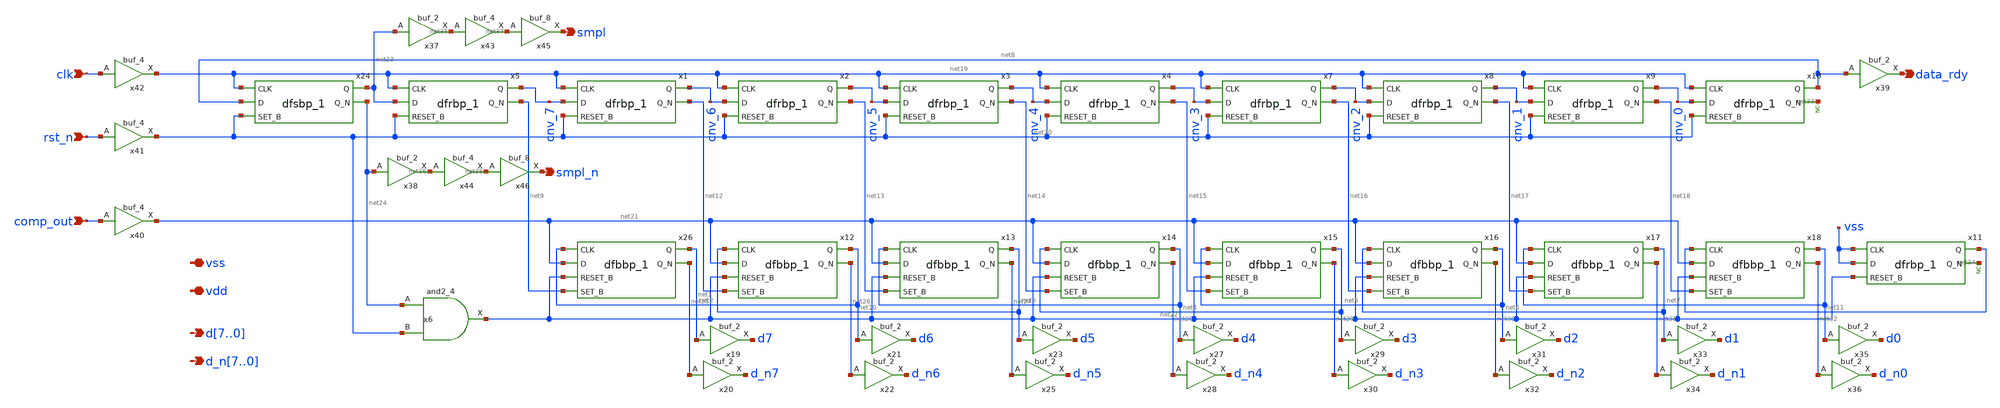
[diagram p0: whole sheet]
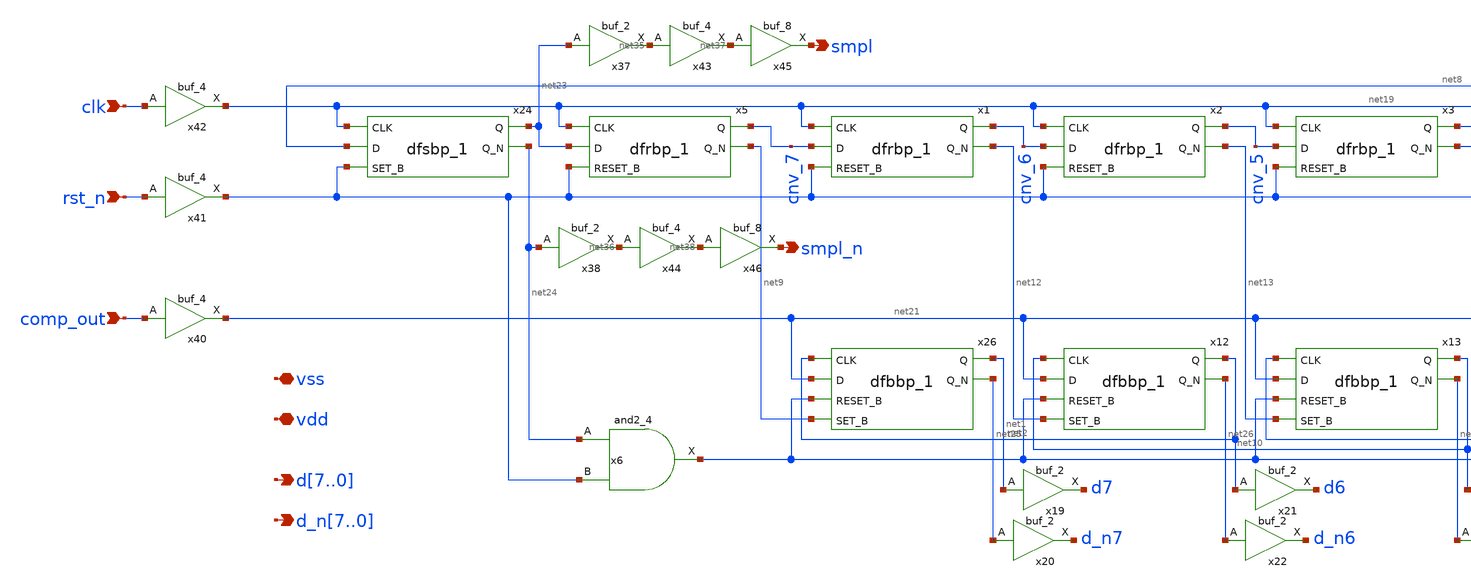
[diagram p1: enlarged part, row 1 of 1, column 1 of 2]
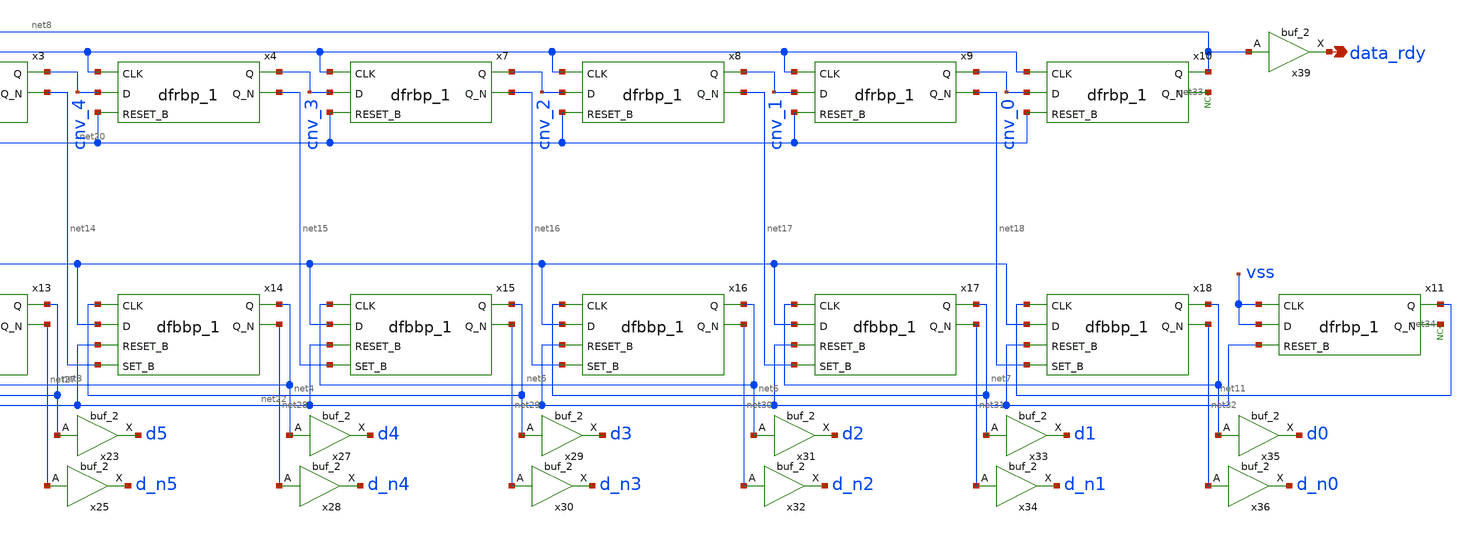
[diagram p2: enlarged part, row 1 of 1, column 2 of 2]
** sch_path: top/test/design/sar_controller.sch
**.subckt sar_controller rst_n data_rdy clk comp_out vss vdd d7,d6,d5,d4,d3,d2,d1,d0
*+ d_n7,d_n6,d_n5,d_n4,d_n3,d_n2,d_n1,d_n0 smpl_n smpl
*.ipin rst_n
*.opin data_rdy
*.ipin clk
*.ipin comp_out
*.iopin vss
*.iopin vdd
*.opin d7,d6,d5,d4,d3,d2,d1,d0
*.opin d_n7,d_n6,d_n5,d_n4,d_n3,d_n2,d_n1,d_n0
*.opin smpl_n
*.opin smpl
x26 net2 net21 net22 net9 vss vss vdd vdd net1 net25 sky130_fd_sc_hd__dfbbp_1
x5 net19 net23 net20 vss vss vdd vdd cnv_7 net9 sky130_fd_sc_hd__dfrbp_1
* noconn #net33
x24 net19 net8 net20 vss vss vdd vdd net23 net24 sky130_fd_sc_hd__dfsbp_1
x6 net24 net20 vss vss vdd vdd net22 sky130_fd_sc_hd__and2_4
x1 net19 cnv_7 net20 vss vss vdd vdd cnv_6 net12 sky130_fd_sc_hd__dfrbp_1
x2 net19 cnv_6 net20 vss vss vdd vdd cnv_5 net13 sky130_fd_sc_hd__dfrbp_1
x3 net19 cnv_5 net20 vss vss vdd vdd cnv_4 net14 sky130_fd_sc_hd__dfrbp_1
x4 net19 cnv_4 net20 vss vss vdd vdd cnv_3 net15 sky130_fd_sc_hd__dfrbp_1
x7 net19 cnv_3 net20 vss vss vdd vdd cnv_2 net16 sky130_fd_sc_hd__dfrbp_1
x8 net19 cnv_2 net20 vss vss vdd vdd cnv_1 net17 sky130_fd_sc_hd__dfrbp_1
x9 net19 cnv_1 net20 vss vss vdd vdd cnv_0 net18 sky130_fd_sc_hd__dfrbp_1
x10 net19 cnv_0 net20 vss vss vdd vdd net8 net33 sky130_fd_sc_hd__dfrbp_1
x11 vss vss net22 vss vss vdd vdd net11 net34 sky130_fd_sc_hd__dfrbp_1
x12 net10 net21 net22 net12 vss vss vdd vdd net2 net26 sky130_fd_sc_hd__dfbbp_1
x13 net3 net21 net22 net13 vss vss vdd vdd net10 net27 sky130_fd_sc_hd__dfbbp_1
x14 net4 net21 net22 net14 vss vss vdd vdd net3 net28 sky130_fd_sc_hd__dfbbp_1
x15 net5 net21 net22 net15 vss vss vdd vdd net4 net29 sky130_fd_sc_hd__dfbbp_1
x16 net6 net21 net22 net16 vss vss vdd vdd net5 net30 sky130_fd_sc_hd__dfbbp_1
x17 net7 net21 net22 net17 vss vss vdd vdd net6 net31 sky130_fd_sc_hd__dfbbp_1
x18 net11 net21 net22 net18 vss vss vdd vdd net7 net32 sky130_fd_sc_hd__dfbbp_1
* noconn #net34
x19 net1 vss vss vdd vdd d7 sky130_fd_sc_hd__buf_2
x20 net25 vss vss vdd vdd d_n7 sky130_fd_sc_hd__buf_2
x21 net2 vss vss vdd vdd d6 sky130_fd_sc_hd__buf_2
x22 net26 vss vss vdd vdd d_n6 sky130_fd_sc_hd__buf_2
x23 net10 vss vss vdd vdd d5 sky130_fd_sc_hd__buf_2
x25 net27 vss vss vdd vdd d_n5 sky130_fd_sc_hd__buf_2
x27 net3 vss vss vdd vdd d4 sky130_fd_sc_hd__buf_2
x28 net28 vss vss vdd vdd d_n4 sky130_fd_sc_hd__buf_2
x29 net4 vss vss vdd vdd d3 sky130_fd_sc_hd__buf_2
x30 net29 vss vss vdd vdd d_n3 sky130_fd_sc_hd__buf_2
x31 net5 vss vss vdd vdd d2 sky130_fd_sc_hd__buf_2
x32 net30 vss vss vdd vdd d_n2 sky130_fd_sc_hd__buf_2
x33 net6 vss vss vdd vdd d1 sky130_fd_sc_hd__buf_2
x34 net31 vss vss vdd vdd d_n1 sky130_fd_sc_hd__buf_2
x35 net7 vss vss vdd vdd d0 sky130_fd_sc_hd__buf_2
x36 net32 vss vss vdd vdd d_n0 sky130_fd_sc_hd__buf_2
x37 net23 vss vss vdd vdd net35 sky130_fd_sc_hd__buf_2
x38 net24 vss vss vdd vdd net36 sky130_fd_sc_hd__buf_2
x39 net8 vss vss vdd vdd data_rdy sky130_fd_sc_hd__buf_2
x40 comp_out vss vss vdd vdd net21 sky130_fd_sc_hd__buf_4
x41 rst_n vss vss vdd vdd net20 sky130_fd_sc_hd__buf_4
x42 clk vss vss vdd vdd net19 sky130_fd_sc_hd__buf_4
x43 net35 vss vss vdd vdd net37 sky130_fd_sc_hd__buf_4
x44 net36 vss vss vdd vdd net38 sky130_fd_sc_hd__buf_4
x45 net37 vss vss vdd vdd smpl sky130_fd_sc_hd__buf_8
x46 net38 vss vss vdd vdd smpl_n sky130_fd_sc_hd__buf_8
**.ends
.end
